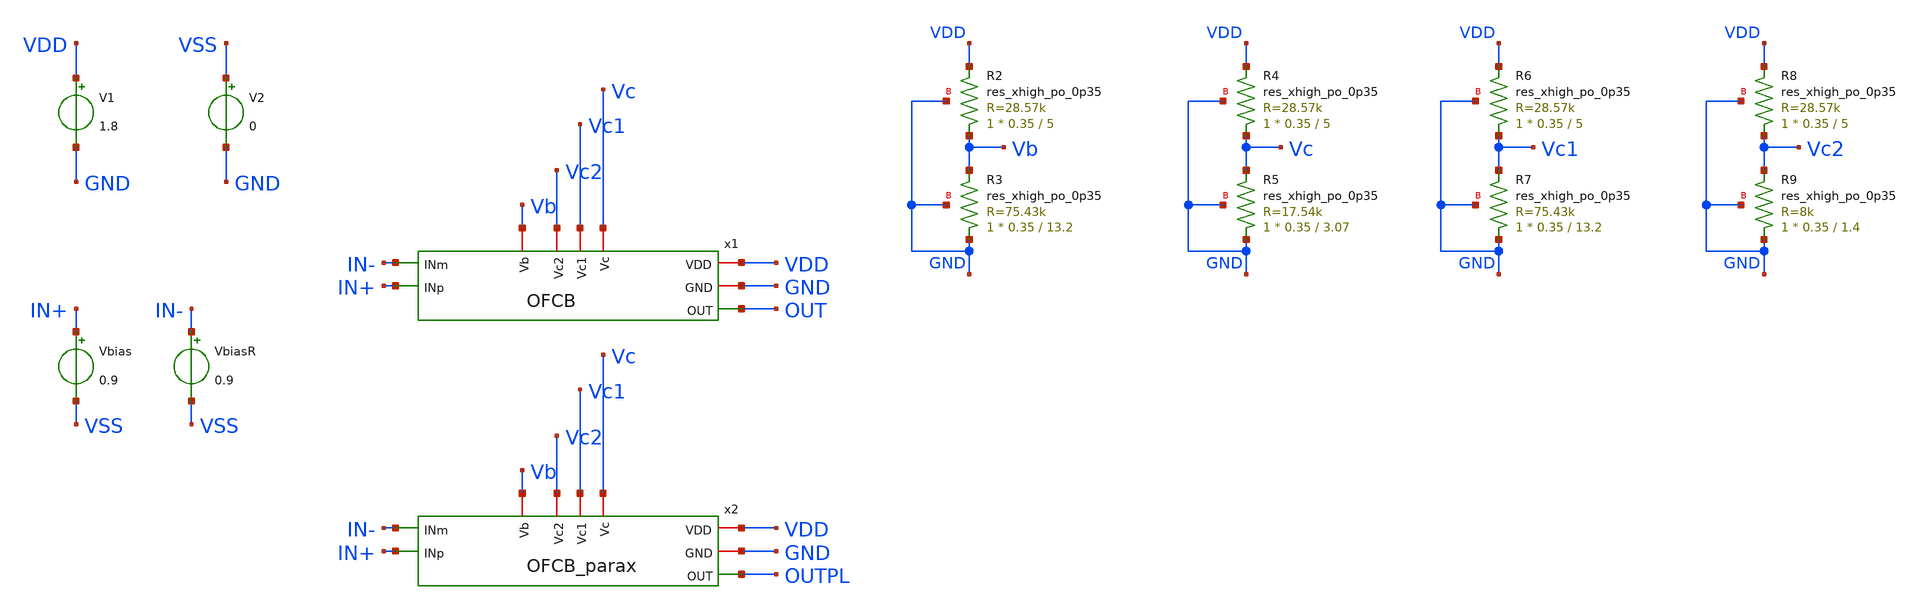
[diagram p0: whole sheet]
** sch_path: xschem/OTA_FoldedCascode1.sch
**.subckt OTA_FoldedCascode1
V1 VDD GND 1.8
Vbias IN+ VSS 0.9
VbiasR IN- VSS 0.9
V2 VSS GND 0
x1 Vb VDD GND Vc2 OUT IN+ IN- Vc1 Vc OFCB
x2 Vb VDD GND Vc2 OUTPL IN+ IN- Vc1 Vc OFCB_parax
XR2 Vb VDD GND sky130_fd_pr__res_xhigh_po_0p35 L=5 mult=1 m=1
XR3 GND Vb GND sky130_fd_pr__res_xhigh_po_0p35 L=13.2 mult=1 m=1
XR4 Vc VDD GND sky130_fd_pr__res_xhigh_po_0p35 L=5 mult=1 m=1
XR5 GND Vc GND sky130_fd_pr__res_xhigh_po_0p35 L=3.07 mult=1 m=1
XR6 Vc1 VDD GND sky130_fd_pr__res_xhigh_po_0p35 L=5 mult=1 m=1
XR7 GND Vc1 GND sky130_fd_pr__res_xhigh_po_0p35 L=13.2 mult=1 m=1
XR8 Vc2 VDD GND sky130_fd_pr__res_xhigh_po_0p35 L=5 mult=1 m=1
XR9 GND Vc2 GND sky130_fd_pr__res_xhigh_po_0p35 L=1.4 mult=1 m=1
**** begin user architecture code



* ngspice commands

.options savecurrents

.control
   set wr_vecnames

   op
   remzerovec
   write OTA_FoldedCascode1.raw
   set appendwrite
   dc Vbias 0.899 0.901 0.00001
   *dc Vbias 0.899 0.901 0.0001
   *dc Vbias 0 1.8 0.01
   *remzerovec
   plot v(out),v(outpl)
   plot deriv(v(out)),deriv(v(outpl))

   write OTA_FoldedCascode1.raw
   wrdata PostLayout_DC_OFCB.txt v(out),v(outpl),deriv(v(out)),deriv(v(outpl))
.endc
.end



.lib $::SKYWATER_MODELS/sky130.lib.spice tt
**** end user architecture code
**.ends

* expanding   symbol:  OFCB.sym # of pins=9
** sym_path: xschem/OFCB.sym
** sch_path: xschem/OFCB.sch
.subckt OFCB Vb VDD GND Vc2 OUT INp INm Vc1 Vc
*.iopin VDD
*.iopin GND
*.opin OUT
*.ipin INp
*.ipin INm
*.iopin Vc2
*.iopin Vc1
*.iopin Vc
*.iopin Vb
XM11 S Vb VDD VDD sky130_fd_pr__pfet_01v8_lvt L=1 W=60 nf=6 ad='int((nf+1)/2) * W/nf * 0.29' as='int((nf+2)/2) * W/nf * 0.29'
+ pd='2*int((nf+1)/2) * (W/nf + 0.29)' ps='2*int((nf+2)/2) * (W/nf + 0.29)' nrd='0.29 / W' nrs='0.29 / W'
+ sa=0 sb=0 sd=0 mult=2 m=2
XM1 D1 INp S S sky130_fd_pr__pfet_01v8_lvt L=10 W=25 nf=2 ad='int((nf+1)/2) * W/nf * 0.29' as='int((nf+2)/2) * W/nf * 0.29'
+ pd='2*int((nf+1)/2) * (W/nf + 0.29)' ps='2*int((nf+2)/2) * (W/nf + 0.29)' nrd='0.29 / W' nrs='0.29 / W'
+ sa=0 sb=0 sd=0 mult=2 m=2
XM2 D2 INm S S sky130_fd_pr__pfet_01v8_lvt L=10 W=25 nf=2 ad='int((nf+1)/2) * W/nf * 0.29' as='int((nf+2)/2) * W/nf * 0.29'
+ pd='2*int((nf+1)/2) * (W/nf + 0.29)' ps='2*int((nf+2)/2) * (W/nf + 0.29)' nrd='0.29 / W' nrs='0.29 / W'
+ sa=0 sb=0 sd=0 mult=2 m=2
XM3 OUT Vc1 D2 GND sky130_fd_pr__nfet_01v8_lvt L=1 W=4 nf=1 ad='int((nf+1)/2) * W/nf * 0.29' as='int((nf+2)/2) * W/nf * 0.29'
+ pd='2*int((nf+1)/2) * (W/nf + 0.29)' ps='2*int((nf+2)/2) * (W/nf + 0.29)' nrd='0.29 / W' nrs='0.29 / W'
+ sa=0 sb=0 sd=0 mult=1 m=1
XM4 D2 Vc GND GND sky130_fd_pr__nfet_01v8_lvt L=1 W=2.8 nf=1 ad='int((nf+1)/2) * W/nf * 0.29' as='int((nf+2)/2) * W/nf * 0.29'
+ pd='2*int((nf+1)/2) * (W/nf + 0.29)' ps='2*int((nf+2)/2) * (W/nf + 0.29)' nrd='0.29 / W' nrs='0.29 / W'
+ sa=0 sb=0 sd=0 mult=1 m=1
XM5 D1 Vc GND GND sky130_fd_pr__nfet_01v8_lvt L=1 W=2.8 nf=1 ad='int((nf+1)/2) * W/nf * 0.29' as='int((nf+2)/2) * W/nf * 0.29'
+ pd='2*int((nf+1)/2) * (W/nf + 0.29)' ps='2*int((nf+2)/2) * (W/nf + 0.29)' nrd='0.29 / W' nrs='0.29 / W'
+ sa=0 sb=0 sd=0 mult=1 m=1
XM6 G Vc1 D1 GND sky130_fd_pr__nfet_01v8_lvt L=1 W=4 nf=1 ad='int((nf+1)/2) * W/nf * 0.29' as='int((nf+2)/2) * W/nf * 0.29'
+ pd='2*int((nf+1)/2) * (W/nf + 0.29)' ps='2*int((nf+2)/2) * (W/nf + 0.29)' nrd='0.29 / W' nrs='0.29 / W'
+ sa=0 sb=0 sd=0 mult=1 m=1
XM7 G Vc2 D9 D9 sky130_fd_pr__pfet_01v8_lvt L=2.23 W=4 nf=1 ad='int((nf+1)/2) * W/nf * 0.29' as='int((nf+2)/2) * W/nf * 0.29'
+ pd='2*int((nf+1)/2) * (W/nf + 0.29)' ps='2*int((nf+2)/2) * (W/nf + 0.29)' nrd='0.29 / W' nrs='0.29 / W'
+ sa=0 sb=0 sd=0 mult=1 m=1
XM9 D9 G VDD VDD sky130_fd_pr__pfet_01v8_lvt L=2.23 W=3.85 nf=1 ad='int((nf+1)/2) * W/nf * 0.29' as='int((nf+2)/2) * W/nf * 0.29'
+ pd='2*int((nf+1)/2) * (W/nf + 0.29)' ps='2*int((nf+2)/2) * (W/nf + 0.29)' nrd='0.29 / W' nrs='0.29 / W'
+ sa=0 sb=0 sd=0 mult=1 m=1
XM8 D10 G VDD VDD sky130_fd_pr__pfet_01v8_lvt L=2.23 W=3.85 nf=1 ad='int((nf+1)/2) * W/nf * 0.29' as='int((nf+2)/2) * W/nf * 0.29'
+ pd='2*int((nf+1)/2) * (W/nf + 0.29)' ps='2*int((nf+2)/2) * (W/nf + 0.29)' nrd='0.29 / W' nrs='0.29 / W'
+ sa=0 sb=0 sd=0 mult=1 m=1
XM10 OUT Vc2 D10 D10 sky130_fd_pr__pfet_01v8_lvt L=2.23 W=4 nf=1 ad='int((nf+1)/2) * W/nf * 0.29' as='int((nf+2)/2) * W/nf * 0.29'
+ pd='2*int((nf+1)/2) * (W/nf + 0.29)' ps='2*int((nf+2)/2) * (W/nf + 0.29)' nrd='0.29 / W' nrs='0.29 / W'
+ sa=0 sb=0 sd=0 mult=1 m=1
XC1 OUT D1 sky130_fd_pr__cap_mim_m3_1 W=22.4 L=22.4 MF=2 m=2
.ends


* expanding   symbol:  OFCB_parax.sym # of pins=9
** sym_path: xschem/OFCB.sym
.include [file normalize ../mag/OFCB.sim.spice]
.end
